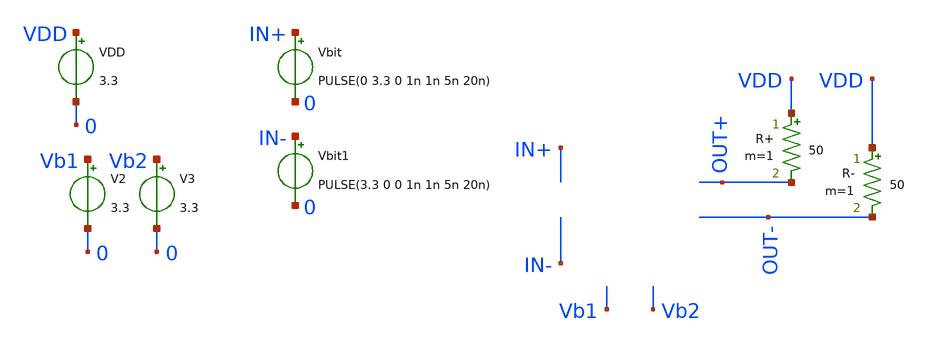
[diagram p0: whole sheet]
** sch_path: chipathon_2023/initial_notebooks_2023/accepted_notebooks/Current-Steering-DAC/DAC/Test_CU.sch
**.subckt Test_CU
Vbit IN+ 0 PULSE(0 3.3 0 1n 1n 5n 20n)
V2 Vb1 0 3.3
V3 Vb2 0 3.3
VDD VDD 0 3.3
Vbit1 IN- 0 PULSE(3.3 0 0 1n 1n 5n 20n)
R+ VDD OUT+ 50 m=1
R- VDD OUT- 50 m=1
**** begin user architecture code




.include /foss/pdks/gf180mcuC/libs.tech/ngspice/design.ngspice
.lib /foss/pdks/gf180mcuC/libs.tech/ngspice/sm141064.ngspice typical


.control
	tran 1n 100n
	*dc vin1 0 3.3 0.1
	plot v(vdd)-v(out+) v(out-)
	*plot v(vout)
.endc
.save all




**** end user architecture code
**.ends
.end
